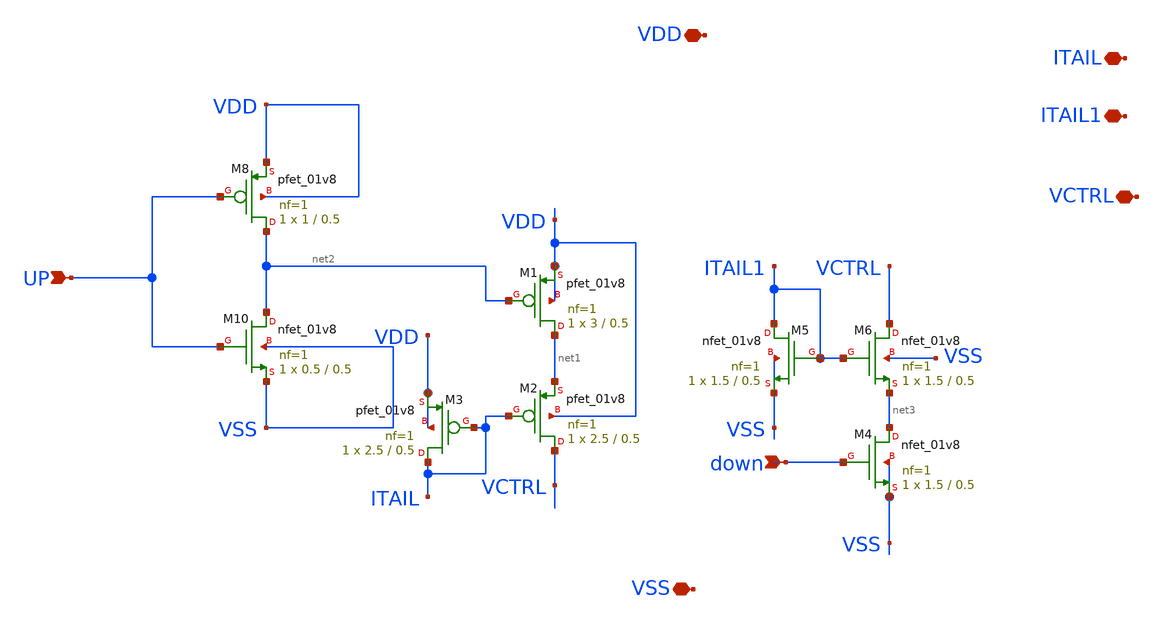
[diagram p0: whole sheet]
** sch_path: Xschem/CP_LP_PFD/CP.sch
**.subckt CP UP down VCTRL VDD VSS ITAIL1 ITAIL
*.ipin UP
*.ipin down
*.iopin VCTRL
*.iopin VDD
*.iopin VSS
*.iopin ITAIL1
*.iopin ITAIL
XM8 net2 UP VDD VDD sky130_fd_pr__pfet_01v8 L=0.5 W=1 nf=1 ad='int((nf+1)/2) * W/nf * 0.29' as='int((nf+2)/2) * W/nf * 0.29'
+ pd='2*int((nf+1)/2) * (W/nf + 0.29)' ps='2*int((nf+2)/2) * (W/nf + 0.29)' nrd='0.29 / W' nrs='0.29 / W'
+ sa=0 sb=0 sd=0 mult=1 m=1
XM1 net1 net2 VDD VDD sky130_fd_pr__pfet_01v8 L=0.5 W=3 nf=1 ad='int((nf+1)/2) * W/nf * 0.29' as='int((nf+2)/2) * W/nf * 0.29'
+ pd='2*int((nf+1)/2) * (W/nf + 0.29)' ps='2*int((nf+2)/2) * (W/nf + 0.29)' nrd='0.29 / W' nrs='0.29 / W'
+ sa=0 sb=0 sd=0 mult=1 m=1
XM10 net2 UP VSS VSS sky130_fd_pr__nfet_01v8 L=0.5 W=0.5 nf=1 ad='int((nf+1)/2) * W/nf * 0.29' as='int((nf+2)/2) * W/nf * 0.29'
+ pd='2*int((nf+1)/2) * (W/nf + 0.29)' ps='2*int((nf+2)/2) * (W/nf + 0.29)' nrd='0.29 / W' nrs='0.29 / W'
+ sa=0 sb=0 sd=0 mult=1 m=1
XM2 VCTRL ITAIL net1 VDD sky130_fd_pr__pfet_01v8 L=0.5 W=2.5 nf=1 ad='int((nf+1)/2) * W/nf * 0.29' as='int((nf+2)/2) * W/nf * 0.29'
+ pd='2*int((nf+1)/2) * (W/nf + 0.29)' ps='2*int((nf+2)/2) * (W/nf + 0.29)' nrd='0.29 / W' nrs='0.29 / W'
+ sa=0 sb=0 sd=0 mult=1 m=1
XM3 ITAIL ITAIL VDD VDD sky130_fd_pr__pfet_01v8 L=0.5 W=2.5 nf=1 ad='int((nf+1)/2) * W/nf * 0.29' as='int((nf+2)/2) * W/nf * 0.29'
+ pd='2*int((nf+1)/2) * (W/nf + 0.29)' ps='2*int((nf+2)/2) * (W/nf + 0.29)' nrd='0.29 / W' nrs='0.29 / W'
+ sa=0 sb=0 sd=0 mult=1 m=1
XM5 ITAIL1 ITAIL1 VSS VSS sky130_fd_pr__nfet_01v8 L=0.5 W=1.5 nf=1 ad='int((nf+1)/2) * W/nf * 0.29' as='int((nf+2)/2) * W/nf * 0.29'
+ pd='2*int((nf+1)/2) * (W/nf + 0.29)' ps='2*int((nf+2)/2) * (W/nf + 0.29)' nrd='0.29 / W' nrs='0.29 / W'
+ sa=0 sb=0 sd=0 mult=1 m=1
XM6 VCTRL ITAIL1 net3 VSS sky130_fd_pr__nfet_01v8 L=0.5 W=1.5 nf=1 ad='int((nf+1)/2) * W/nf * 0.29' as='int((nf+2)/2) * W/nf * 0.29'
+ pd='2*int((nf+1)/2) * (W/nf + 0.29)' ps='2*int((nf+2)/2) * (W/nf + 0.29)' nrd='0.29 / W' nrs='0.29 / W'
+ sa=0 sb=0 sd=0 mult=1 m=1
XM4 net3 down VSS VSS sky130_fd_pr__nfet_01v8 L=0.5 W=1.5 nf=1 ad='int((nf+1)/2) * W/nf * 0.29' as='int((nf+2)/2) * W/nf * 0.29'
+ pd='2*int((nf+1)/2) * (W/nf + 0.29)' ps='2*int((nf+2)/2) * (W/nf + 0.29)' nrd='0.29 / W' nrs='0.29 / W'
+ sa=0 sb=0 sd=0 mult=1 m=1
**.ends
.end
